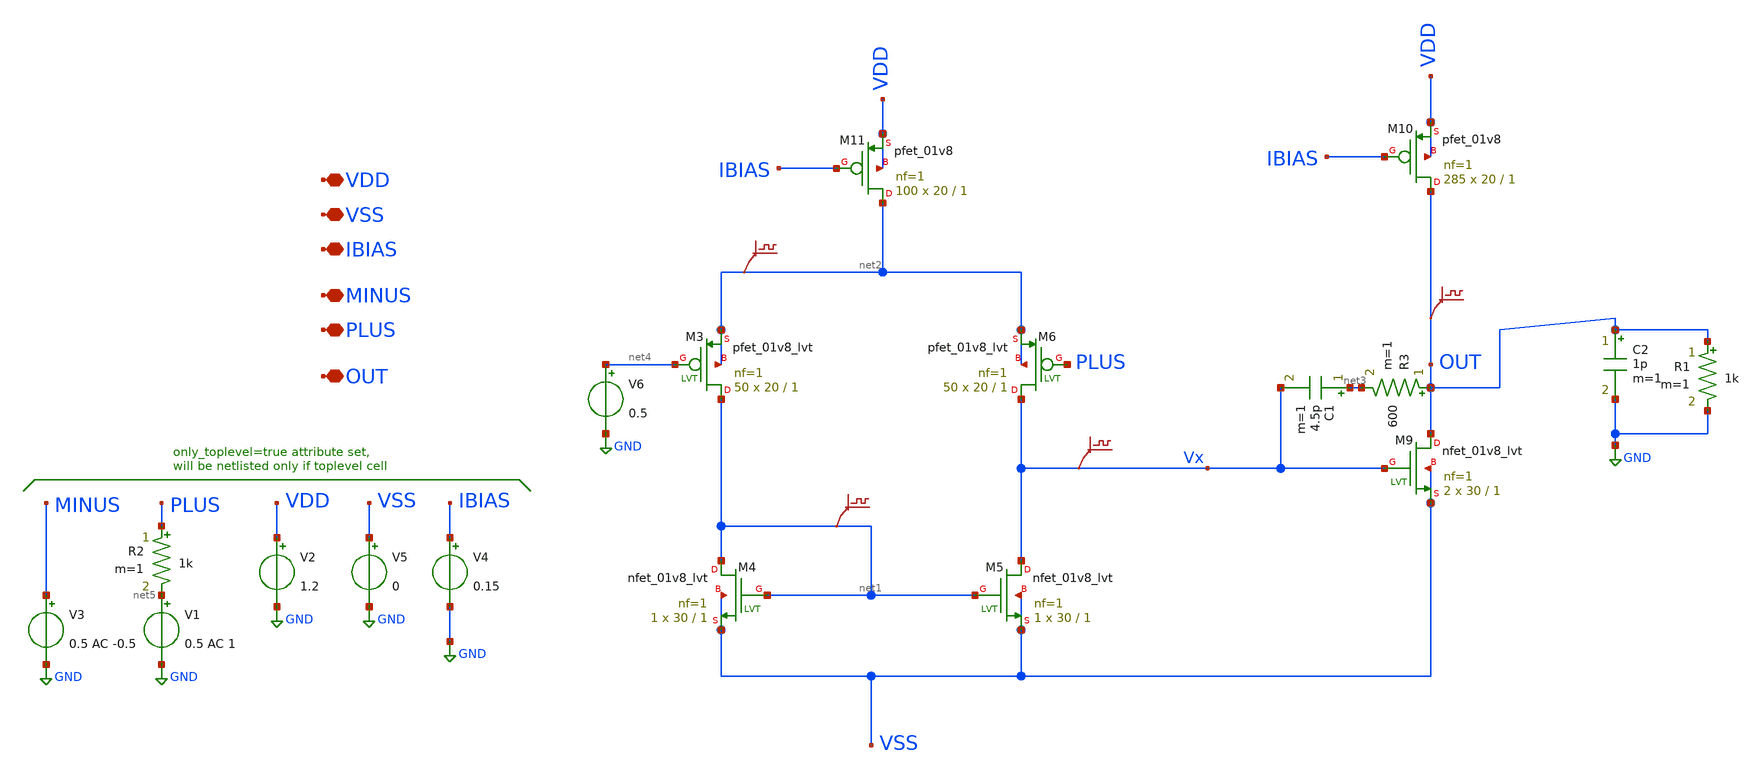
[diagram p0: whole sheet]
** sch_path: q2_opamp.sch
**.subckt q2_opamp VDD VSS MINUS PLUS OUT IBIAS
*.iopin VDD
*.iopin VSS
*.iopin MINUS
*.iopin PLUS
*.iopin OUT
*.iopin IBIAS
V3 MINUS GND 0.5 AC -0.5
V5 VSS GND 0
V2 VDD GND 1.2
.save v(vx)
XM4 net1 net1 VSS VSS sky130_fd_pr__nfet_01v8_lvt L=1 W=30 nf=1 ad='int((nf+1)/2) * W/nf * 0.29' as='int((nf+2)/2) * W/nf * 0.29'
+ pd='2*int((nf+1)/2) * (W/nf + 0.29)' ps='2*int((nf+2)/2) * (W/nf + 0.29)' nrd='0.29 / W' nrs='0.29 / W'
+ sa=0 sb=0 sd=0 mult=1 m=1
XM5 Vx net1 VSS VSS sky130_fd_pr__nfet_01v8_lvt L=1 W=30 nf=1 ad='int((nf+1)/2) * W/nf * 0.29' as='int((nf+2)/2) * W/nf * 0.29'
+ pd='2*int((nf+1)/2) * (W/nf + 0.29)' ps='2*int((nf+2)/2) * (W/nf + 0.29)' nrd='0.29 / W' nrs='0.29 / W'
+ sa=0 sb=0 sd=0 mult=1 m=1
XM3 net1 net4 net2 net2 sky130_fd_pr__pfet_01v8_lvt L=1 W=20 nf=1 ad='int((nf+1)/2) * W/nf * 0.29' as='int((nf+2)/2) * W/nf * 0.29'
+ pd='2*int((nf+1)/2) * (W/nf + 0.29)' ps='2*int((nf+2)/2) * (W/nf + 0.29)' nrd='0.29 / W' nrs='0.29 / W'
+ sa=0 sb=0 sd=0 mult=50 m=50
XM6 Vx PLUS net2 net2 sky130_fd_pr__pfet_01v8_lvt L=1 W=20 nf=1 ad='int((nf+1)/2) * W/nf * 0.29' as='int((nf+2)/2) * W/nf * 0.29'
+ pd='2*int((nf+1)/2) * (W/nf + 0.29)' ps='2*int((nf+2)/2) * (W/nf + 0.29)' nrd='0.29 / W' nrs='0.29 / W'
+ sa=0 sb=0 sd=0 mult=50 m=50
.save v(net2)
XM9 OUT Vx VSS VSS sky130_fd_pr__nfet_01v8_lvt L=1 W=30 nf=1 ad='int((nf+1)/2) * W/nf * 0.29' as='int((nf+2)/2) * W/nf * 0.29'
+ pd='2*int((nf+1)/2) * (W/nf + 0.29)' ps='2*int((nf+2)/2) * (W/nf + 0.29)' nrd='0.29 / W' nrs='0.29 / W'
+ sa=0 sb=0 sd=0 mult=2 m=2
.save v(net1)
.save v(out)
C1 net3 Vx 4.5p m=1
C2 OUT GND 1p m=1
R1 OUT GND 1k m=1
R2 PLUS net5 1k m=1
R3 OUT net3 600 m=1
XM10 OUT IBIAS VDD VDD sky130_fd_pr__pfet_01v8 L=1 W=20 nf=1 ad='int((nf+1)/2) * W/nf * 0.29' as='int((nf+2)/2) * W/nf * 0.29'
+ pd='2*int((nf+1)/2) * (W/nf + 0.29)' ps='2*int((nf+2)/2) * (W/nf + 0.29)' nrd='0.29 / W' nrs='0.29 / W'
+ sa=0 sb=0 sd=0 mult=285 m=285
XM11 net2 IBIAS VDD VDD sky130_fd_pr__pfet_01v8 L=1 W=20 nf=1 ad='int((nf+1)/2) * W/nf * 0.29' as='int((nf+2)/2) * W/nf * 0.29'
+ pd='2*int((nf+1)/2) * (W/nf + 0.29)' ps='2*int((nf+2)/2) * (W/nf + 0.29)' nrd='0.29 / W' nrs='0.29 / W'
+ sa=0 sb=0 sd=0 mult=100 m=100
V4 IBIAS GND 0.15
V1 net5 GND 0.5 AC 1
V6 net4 GND 0.5
**** begin user architecture code

** opencircuitdesign pdks install
.lib $::SKYWATER_MODELS/sky130.lib.spice tt





.control

ac dec 20 1 10000000g
*run
plot db(v(out)) 180*cph(v(out))/pi
*plot db(v(Vx)) 180*cph(v(Vx))/pi
*reset
*tran 100n 10m
*dc v1 0.2 0.8 0.001
*plot out
setplot tran1
plot vout
*plot v(out) v(plus)

save @m.xm5.msky130_fd_pr__nfet_01v8_lvt[gm]
save @m.xm5.msky130_fd_pr__nfet_01v8_lvt[vth]
save @m.xm5.msky130_fd_pr__nfet_01v8_lvt[vdsat]
save @m.xm5.msky130_fd_pr__nfet_01v8_lvt[vds]
save @m.xm5.msky130_fd_pr__nfet_01v8_lvt[id]
save @m.xm5.msky130_fd_pr__nfet_01v8_lvt[gds]
save @m.xm5.msky130_fd_pr__nfet_01v8_lvt[cgg]
save @m.xm5.msky130_fd_pr__nfet_01v8_lvt[cgd]

save @m.xm6.msky130_fd_pr__pfet_01v8_lvt[gm]
save @m.xm6.msky130_fd_pr__pfet_01v8_lvt[vth]
save @m.xm6.msky130_fd_pr__pfet_01v8_lvt[vdsat]
save @m.xm6.msky130_fd_pr__pfet_01v8_lvt[vds]
save @m.xm6.msky130_fd_pr__pfet_01v8_lvt[id]
save @m.xm6.msky130_fd_pr__pfet_01v8_lvt[gds]
save @m.xm6.msky130_fd_pr__pfet_01v8_lvt[cgg]
save @m.xm6.msky130_fd_pr__pfet_01v8_lvt[cgd]

save @m.xm9.msky130_fd_pr__nfet_01v8_lvt[gm]
save @m.xm9.msky130_fd_pr__nfet_01v8_lvt[vth]
save @m.xm9.msky130_fd_pr__nfet_01v8_lvt[vdsat]
save @m.xm9.msky130_fd_pr__nfet_01v8_lvt[vds]
save @m.xm9.msky130_fd_pr__nfet_01v8_lvt[id]
save @m.xm9.msky130_fd_pr__nfet_01v8_lvt[gds]
save @m.xm9.msky130_fd_pr__nfet_01v8_lvt[cgg]
save @m.xm9.msky130_fd_pr__nfet_01v8_lvt[cgd]

save @m.xm10.msky130_fd_pr__pfet_01v8[gm]
save @m.xm10.msky130_fd_pr__pfet_01v8[vth]
save @m.xm10.msky130_fd_pr__pfet_01v8[vdsat]
save @m.xm10.msky130_fd_pr__pfet_01v8[vds]
save @m.xm10.msky130_fd_pr__pfet_01v8[id]
save @m.xm10.msky130_fd_pr__pfet_01v8[gds]
save @m.xm10.msky130_fd_pr__pfet_01v8[cgg]
save @m.xm10.msky130_fd_pr__pfet_01v8[cgd]
save @m.xm10.msky130_fd_pr__pfet_01v8[cdb]

save @m.xm11.msky130_fd_pr__pfet_01v8[gm]
save @m.xm11.msky130_fd_pr__pfet_01v8[vth]
save @m.xm11.msky130_fd_pr__pfet_01v8[vdsat]
save @m.xm11.msky130_fd_pr__pfet_01v8[vds]
save @m.xm11.msky130_fd_pr__pfet_01v8[id]
save @m.xm11.msky130_fd_pr__pfet_01v8[gds]
save @m.xm11.msky130_fd_pr__pfet_01v8[cgg]
save @m.xm11.msky130_fd_pr__pfet_01v8[cgd]

save all
op

write q2_opamp.raw

.endc


**** end user architecture code
**.ends
.GLOBAL GND
.end
